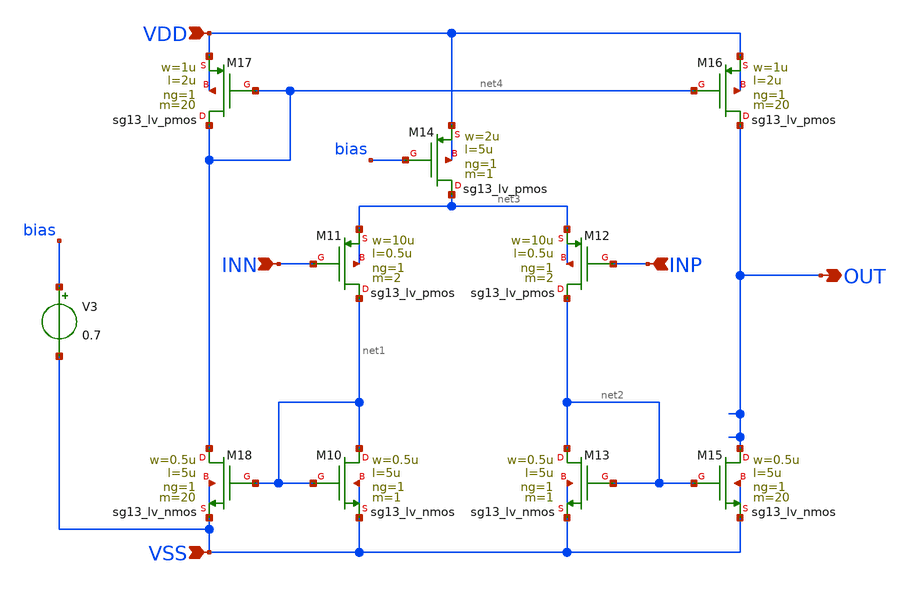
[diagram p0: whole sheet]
** sch_path: ota/ota_int.sch
**.subckt ota_int VDD VSS INN INP OUT
*.ipin VDD
*.ipin VSS
*.ipin INN
*.ipin INP
*.opin OUT
XM10 net1 net1 VSS VSS sg13_lv_nmos w=0.5u l=5u ng=1 m=1 mm_ok=1
XM11 net1 INN net3 net3 sg13_lv_pmos w=10u l=0.5u ng=1 m=2 mm_ok=1
XM12 net2 INP net3 net3 sg13_lv_pmos w=10u l=0.5u ng=1 m=2 mm_ok=1
XM13 net2 net2 VSS VSS sg13_lv_nmos w=0.5u l=5u ng=1 m=1 mm_ok=1
XM14 net3 bias VDD VDD sg13_lv_pmos w=2u l=5u ng=1 m=1 mm_ok=1
XM15 OUT net2 VSS VSS sg13_lv_nmos w=0.5u l=5u ng=1 m=20 mm_ok=1
XM16 OUT net4 VDD VDD sg13_lv_pmos w=1u l=2u ng=1 m=20 mm_ok=1
XM17 net4 net4 VDD VDD sg13_lv_pmos w=1u l=2u ng=1 m=20 mm_ok=1
XM18 net4 net1 VSS VSS sg13_lv_nmos w=0.5u l=5u ng=1 m=20 mm_ok=1
V3 bias VSS 0.7
**.ends
.end
